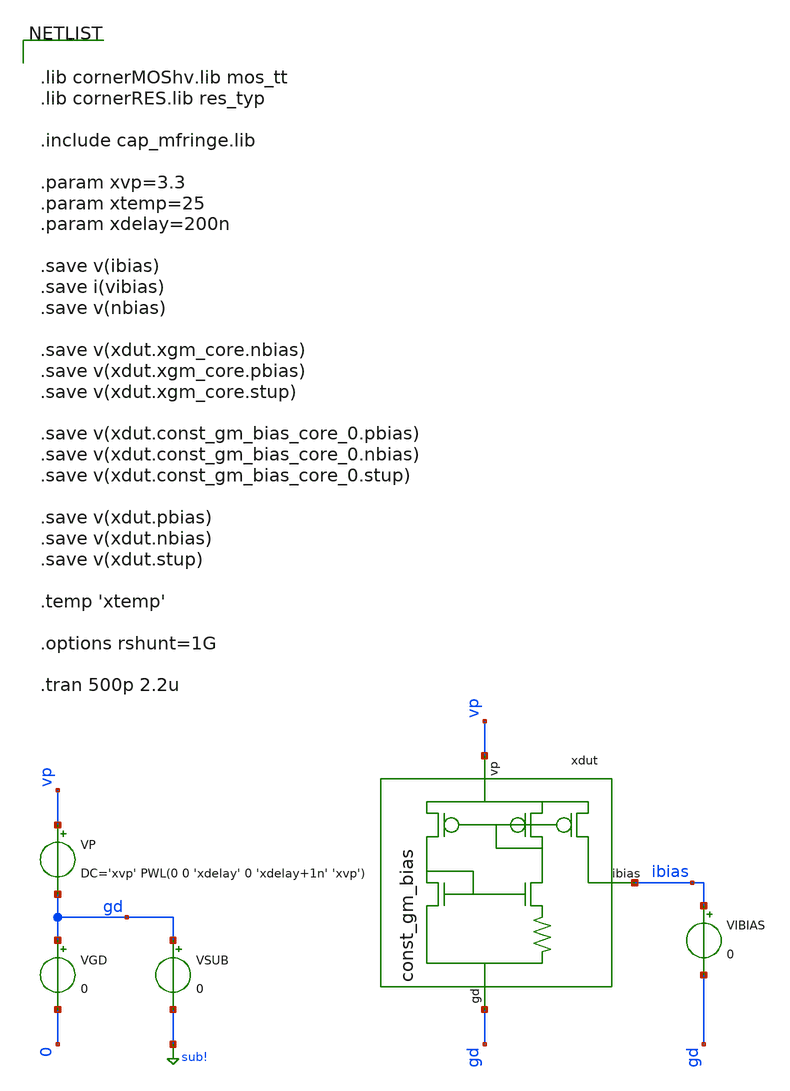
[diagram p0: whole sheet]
** sch_path: testbench/const_gm_bias_startup_tb.sch
**.subckt const_gm_bias_startup_tb
VP vp gd DC='xvp' PWL(0 0 'xdelay' 0 'xdelay+1n' 'xvp')
VGD gd 0 0
VSUB gd sub! 0
xdut vp ibias gd const_gm_bias
VIBIAS ibias gd 0
**** begin user architecture code


.lib cornerMOShv.lib mos_tt
.lib cornerRES.lib res_typ

.include cap_mfringe.lib

.param xvp=3.3
.param xtemp=25
.param xdelay=200n

.save v(ibias)
.save i(vibias)
.save v(nbias)

.save v(xdut.xgm_core.nbias)
.save v(xdut.xgm_core.pbias)
.save v(xdut.xgm_core.stup)

.save v(xdut.const_gm_bias_core_0.pbias)
.save v(xdut.const_gm_bias_core_0.nbias)
.save v(xdut.const_gm_bias_core_0.stup)

.save v(xdut.pbias)
.save v(xdut.nbias)
.save v(xdut.stup)

.temp 'xtemp'

.options rshunt=1G

.tran 500p 2.2u


**** end user architecture code
**.ends

* expanding   symbol:  /foss/designs/test/circuit/const_gm_bias.sym # of pins=3
** sym_path: circuit/const_gm_bias.sym
** sch_path: circuit/const_gm_bias.sch
.subckt const_gm_bias vp ibias gd
*.opin ibias
*.ipin vp
*.ipin gd
xgm_core vp ibias gd vr const_gm_bias_core
XRbias vr gd gd rppd w=1.2e-6 l=11.7e-6 m=1 b=0 mm_ok=1
XR2 gd net1 gd rppd w=1.2e-6 l=3.9e-6 m=1 b=0 mm_ok=1
XR3 net1 gd gd rppd w=1.2e-6 l=1.3e-6 m=1 b=0 mm_ok=1
.ends


* expanding   symbol:  /foss/designs/test/circuit/const_gm_bias_core.sym # of pins=4
** sym_path: circuit/const_gm_bias_core.sym
** sch_path: circuit/const_gm_bias_core.sch
.subckt const_gm_bias_core vp ibias gd res
*.ipin vp
*.ipin gd
*.opin ibias
*.opin res
XM1 net1 nbias gd gd sg13_hv_nmos w=0.6u l=2u ng=1 m=2 mm_ok=1
XM3 net2 nbias res gd sg13_hv_nmos w=0.6u l=2u ng=1 m=4 mm_ok=1
XM8 net5 pbias vp vp sg13_hv_pmos w=0.6u l=2u ng=1 m=2 mm_ok=1
XM6 net4 pbias vp vp sg13_hv_pmos w=0.6u l=2u ng=1 m=2 mm_ok=1
XM10 net3 pbias vp vp sg13_hv_pmos w=0.6u l=2u ng=1 m=2 mm_ok=1
XM13 net6 gd vp vp sg13_hv_pmos w=0.6u l=4.38u ng=1 m=1 mm_ok=1
XM11 stup nbias gd gd sg13_hv_nmos w=0.6u l=2u ng=1 m=4 mm_ok=1
XM800 pbias stup gd gd sg13_hv_nmos w=0.6u l=2u ng=1 m=2 mm_ok=1
XM2 nbias nbias net1 gd sg13_hv_nmos w=0.6u l=2u ng=1 m=2 mm_ok=1
XM4 pbias nbias net2 gd sg13_hv_nmos w=0.6u l=2u ng=1 m=4 mm_ok=1
XM9 ibias pbias net3 vp sg13_hv_pmos w=0.6u l=2u ng=1 m=2 mm_ok=1
XM7 pbias pbias net5 vp sg13_hv_pmos w=0.6u l=2u ng=1 m=2 mm_ok=1
XM5 nbias pbias net4 vp sg13_hv_pmos w=0.6u l=2u ng=1 m=2 mm_ok=1
XM12 stup gd net6 vp sg13_hv_pmos w=0.6u l=4.38u ng=1 m=1 mm_ok=1
.ends

.GLOBAL sub!
.end
